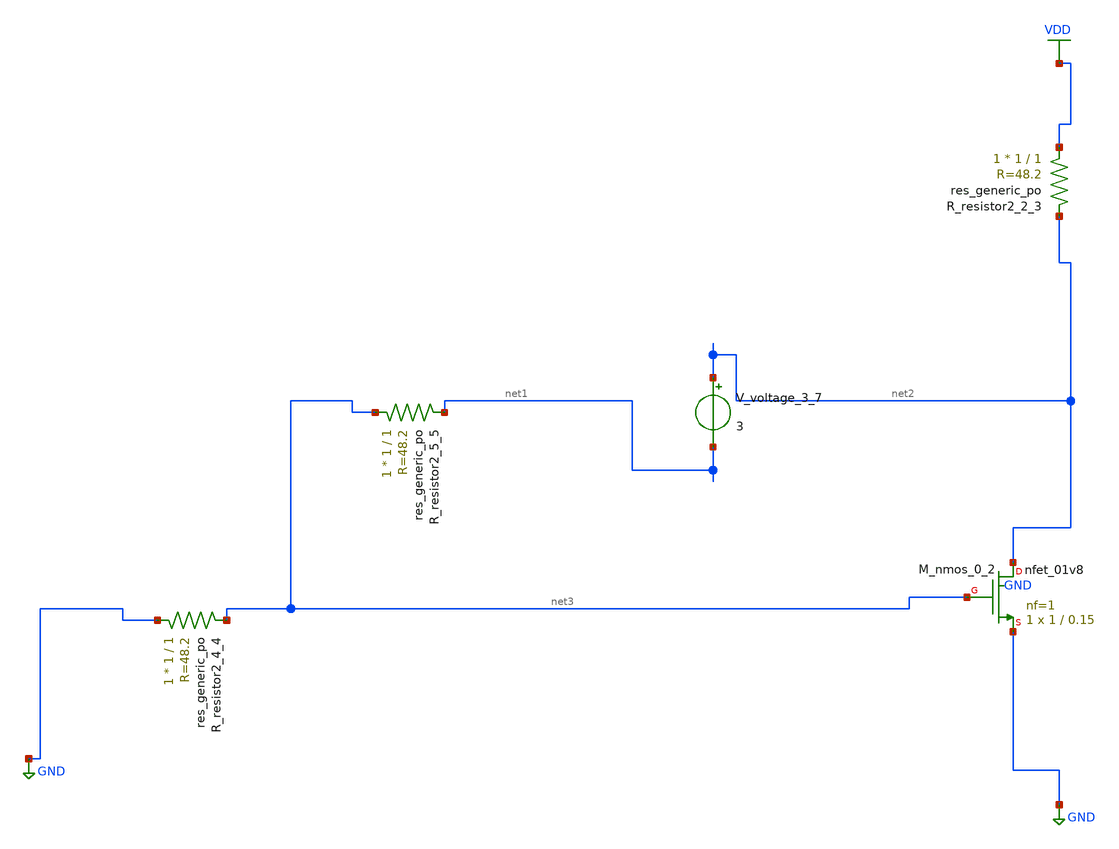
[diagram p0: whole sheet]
** sch_path: schematics/AMSNet/602.sch
**.subckt 602
XM_nmos_0_2 net2 net3 GND GND sky130_fd_pr__nfet_01v8 L=0.15 W=1 nf=1 ad='int((1 + 1)/2) * 1 / 1 * 0.29'
+ as='int((1 + 2)/2) * 1 / 1 * 0.29' pd='2*int((1 + 1)/2) * (1 / 1 + 0.29)' ps='2*int((1 + 2)/2) * (1 / 1 + 0.29)'
+ nrd='0.29 / 1 ' nrs='0.29 / 1 ' sa=0 sb=0 sd=0 mult=1 m=1
XR_resistor2_2_3 VDD net2 sky130_fd_pr__res_generic_po W=1 L=1 m=1
XR_resistor2_4_4 GND net3 sky130_fd_pr__res_generic_po W=1 L=1 m=1
XR_resistor2_5_5 net3 net1 sky130_fd_pr__res_generic_po W=1 L=1 m=1
V_voltage_3_7 net2 net1 3
**.ends
.GLOBAL GND
.GLOBAL VDD
.end
